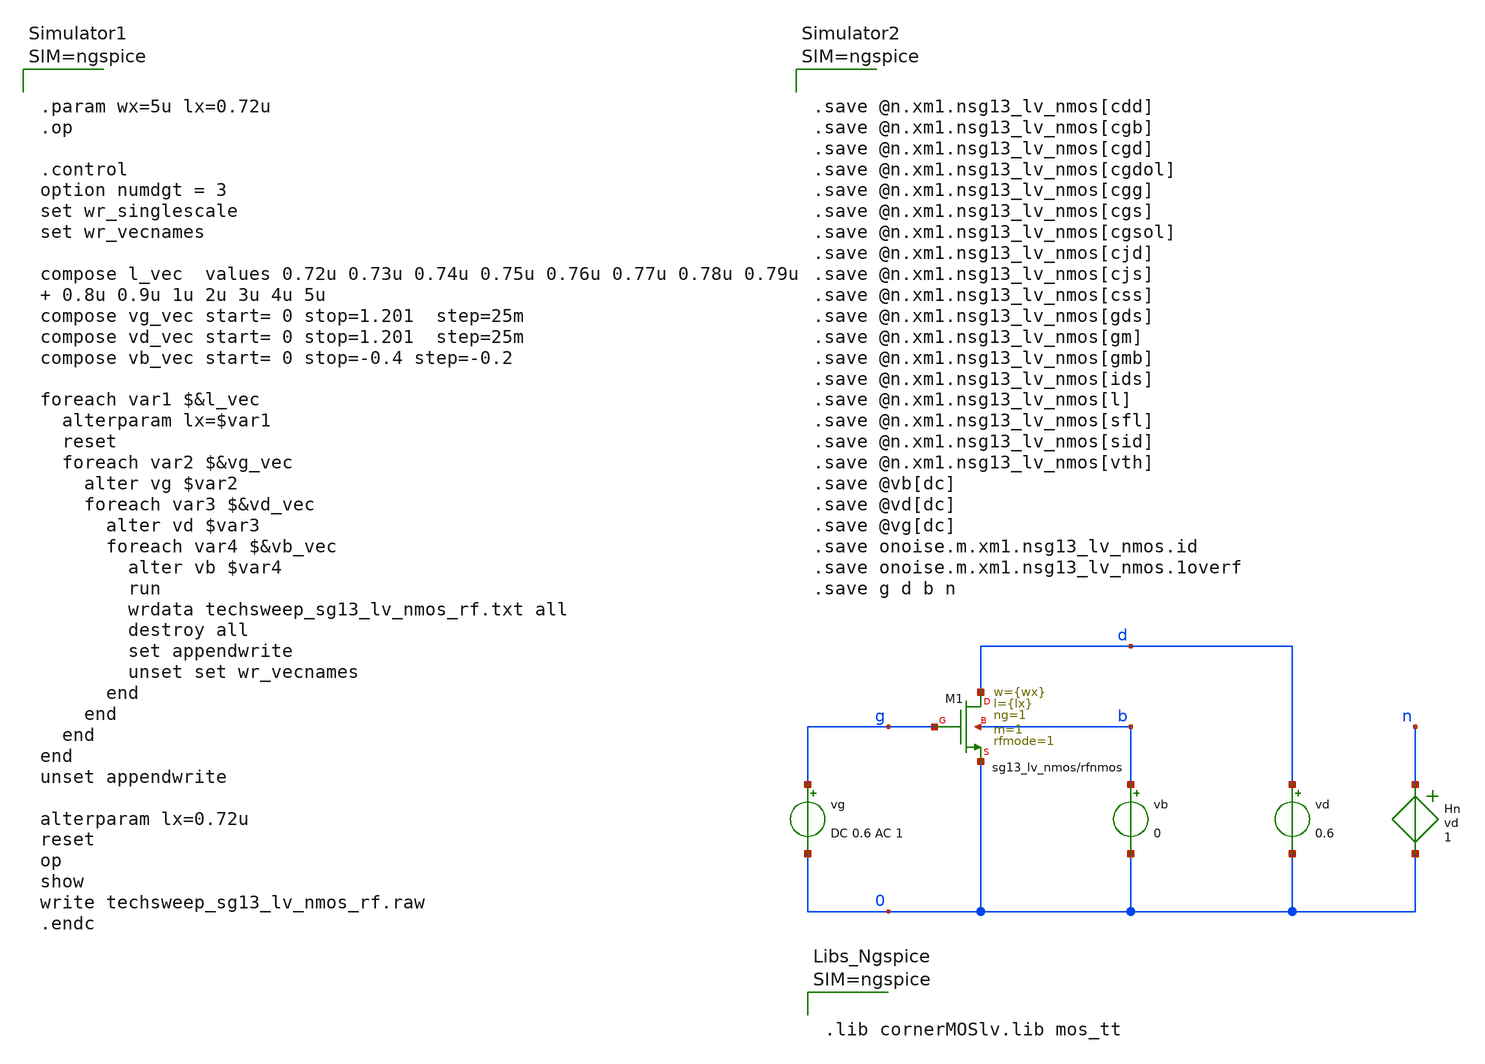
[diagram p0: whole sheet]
** sch_path: starter_files_open_source_tools/ihp-sg13cmos5l/techsweep_sg13_lv_nmos_rf.sch
**.subckt techsweep_sg13_lv_nmos_rf
vg g 0 DC 0.6 AC 1
vb b 0 0
vd d 0 0.6
Hn n 0 vd 1
XM1 d g 0 b sg13_lv_nmos w={wx} l={lx} ng=1 m=1 rfmode=1 mm_ok=1
**** begin user architecture code



.save @n.xm1.nsg13_lv_nmos[cdd]
.save @n.xm1.nsg13_lv_nmos[cgb]
.save @n.xm1.nsg13_lv_nmos[cgd]
.save @n.xm1.nsg13_lv_nmos[cgdol]
.save @n.xm1.nsg13_lv_nmos[cgg]
.save @n.xm1.nsg13_lv_nmos[cgs]
.save @n.xm1.nsg13_lv_nmos[cgsol]
.save @n.xm1.nsg13_lv_nmos[cjd]
.save @n.xm1.nsg13_lv_nmos[cjs]
.save @n.xm1.nsg13_lv_nmos[css]
.save @n.xm1.nsg13_lv_nmos[gds]
.save @n.xm1.nsg13_lv_nmos[gm]
.save @n.xm1.nsg13_lv_nmos[gmb]
.save @n.xm1.nsg13_lv_nmos[ids]
.save @n.xm1.nsg13_lv_nmos[l]
.save @n.xm1.nsg13_lv_nmos[sfl]
.save @n.xm1.nsg13_lv_nmos[sid]
.save @n.xm1.nsg13_lv_nmos[vth]
.save @vb[dc]
.save @vd[dc]
.save @vg[dc]
.save onoise.m.xm1.nsg13_lv_nmos.id
.save onoise.m.xm1.nsg13_lv_nmos.1overf
.save g d b n






.param wx=5u lx=0.72u
.op

.control
option numdgt = 3
set wr_singlescale
set wr_vecnames

compose l_vec  values 0.72u 0.73u 0.74u 0.75u 0.76u 0.77u 0.78u 0.79u  0.8u 0.9u 1u 2u 3u 4u 5u
compose vg_vec start= 0 stop=1.201  step=25m
compose vd_vec start= 0 stop=1.201  step=25m
compose vb_vec start= 0 stop=-0.4 step=-0.2

foreach var1 $&l_vec
  alterparam lx=$var1
  reset
  foreach var2 $&vg_vec
    alter vg $var2
    foreach var3 $&vd_vec
      alter vd $var3
      foreach var4 $&vb_vec
        alter vb $var4
        run
        wrdata techsweep_sg13_lv_nmos_rf.txt all
        destroy all
        set appendwrite
        unset set wr_vecnames
      end
    end
  end
end
unset appendwrite

alterparam lx=0.72u
reset
op
show
write techsweep_sg13_lv_nmos_rf.raw
.endc






.lib cornerMOSlv.lib mos_tt



**** end user architecture code
**.ends
.end
